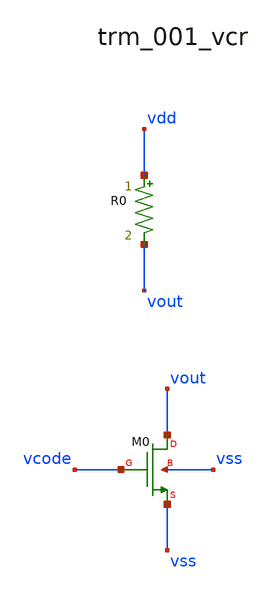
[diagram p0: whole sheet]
** sch_path: analog-db/raw/trm_001_vcr/hier/trm_001_vcr.sch
**.subckt trm_001_vcr
R0 vdd vout x_dut_r0_value m=1
XM0 vout vcode vss vss sg13_lv_nmos w=x_dut_xm0_w l=x_dut_xm0_l ng=1 m=x_dut_xm0_m
**.ends
.end
